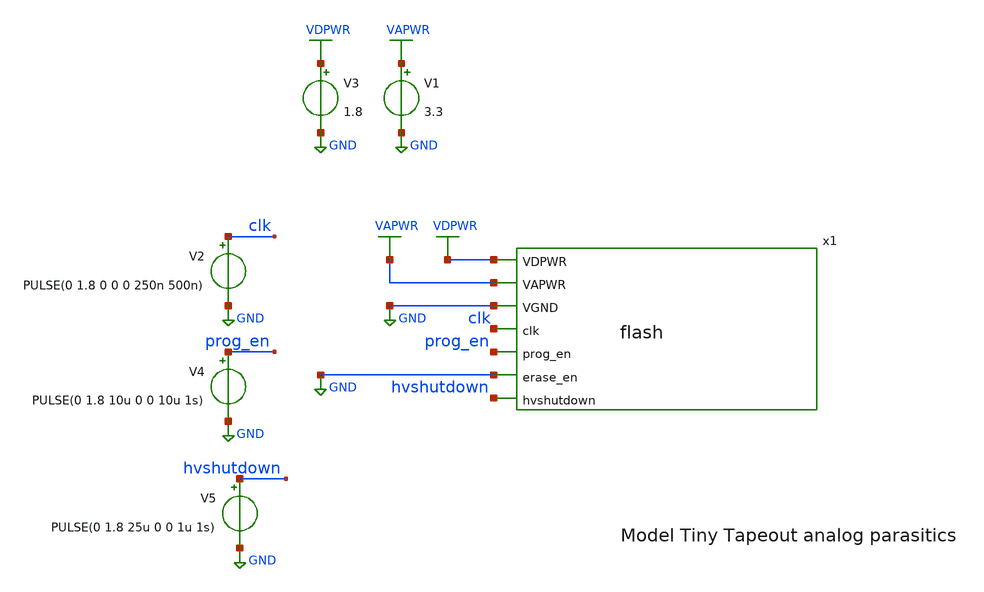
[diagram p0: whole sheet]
** sch_path: xschem/flash_tb.sch
**.subckt flash_tb
V1 VAPWR GND 3.3
V2 clk GND PULSE(0 1.8 0 0 0 250n 500n)
x1 VDPWR VAPWR GND clk prog_en GND hvshutdown flash
V3 VDPWR GND 1.8
V4 prog_en GND PULSE(0 1.8 10u 0 0 10u 1s)
V5 hvshutdown GND PULSE(0 1.8 25u 0 0 1u 1s)
**** begin user architecture code

** opencircuitdesign pdks install
.lib $::SKYWATER_MODELS/sky130.lib.spice tt





.tran 10n 100u
.save all

.control
run
write flash_tb.raw
.endc


**** end user architecture code
**.ends
.GLOBAL GND
.GLOBAL VAPWR
.GLOBAL VDPWR
.end
